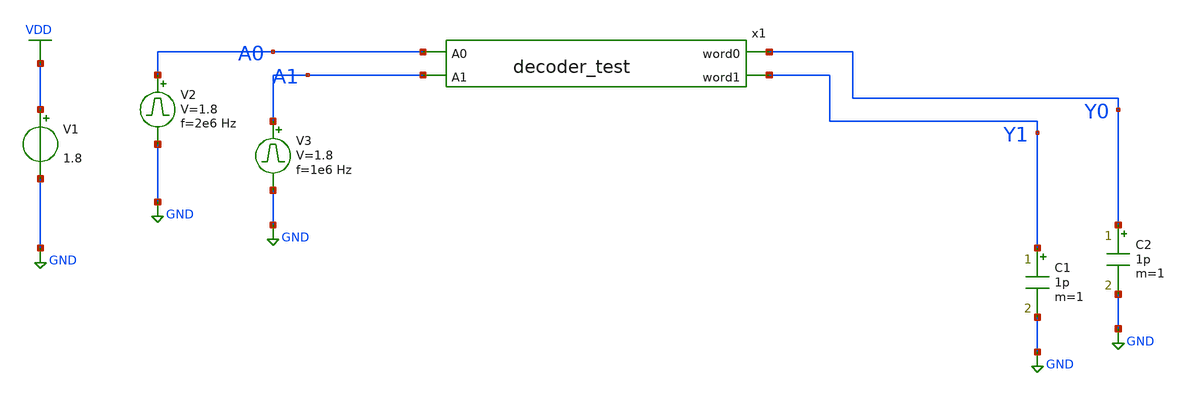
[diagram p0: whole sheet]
** sch_path: circuits/xschem/partials/decoder_test_tb.sch
**.subckt decoder_test_tb
V1 VDD GND 1.8
C1 Y1 GND 1p m=1
C2 Y0 GND 1p m=1
x1 A0 A1 Y0 Y1 decoder_test
V2 A0 GND pulse 0 1.8 '0.495/ 2e6 ' '0.01/2e6 ' '0.01/2e6 ' '0.49/2e6 ' '1/2e6 '
V3 A1 GND pulse 0 1.8 '0.495/ 1e6 ' '0.01/1e6 ' '0.01/1e6 ' '0.49/1e6 ' '1/1e6 '
**** begin user architecture code


.control
save all
tran 1n 2u
plot V(A0) V(A1)+2 V(Y0)+4 V(Y1)+6
.endc



** opencircuitdesign pdks install
.lib $::SKYWATER_MODELS/sky130.lib.spice tt


**** end user architecture code
**.ends
.GLOBAL VDD
.GLOBAL GND
.end
